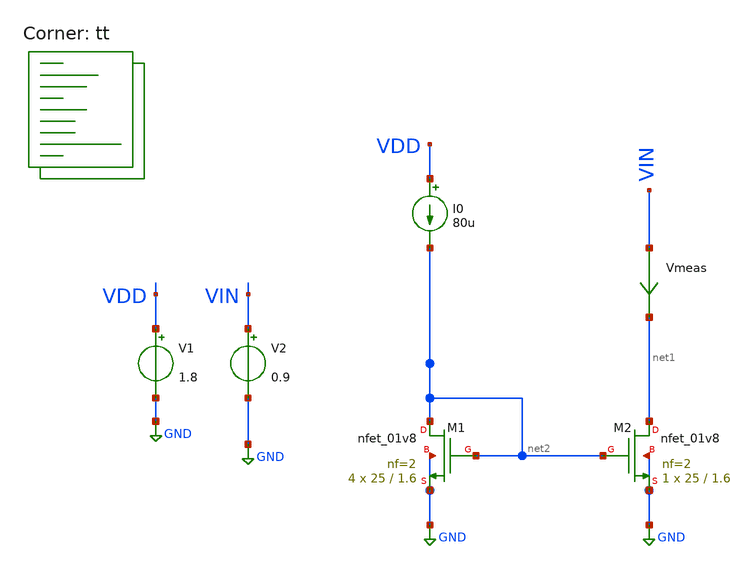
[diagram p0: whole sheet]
** sch_path: sky130B/Analog_integrated_circuit_Design/chapter3/1/1.sch
**.subckt 1
V1 VDD GND 1.8
V2 VIN GND 0.9
Vmeas VIN net1 0
.save i(vmeas)
XM2 net1 net2 GND GND sky130_fd_pr__nfet_01v8 L=1.6 W=25 nf=2 ad='int((2 + 1)/2) * 25 / 2 * 0.29' as='int((2 + 2)/2) * 25 / 2 * 0.29'
+ pd='2*int((2 + 1)/2) * (25 / 2 + 0.29)' ps='2*int((2 + 2)/2) * (25 / 2 + 0.29)' nrd='0.29 / 25 ' nrs='0.29 / 25 '
+ sa=0 sb=0 sd=0 mult=1 m=1
XM1 net2 net2 GND GND sky130_fd_pr__nfet_01v8 L=1.6 W=25 nf=2 ad='int((2 + 1)/2) * 25 / 2 * 0.29' as='int((2 + 2)/2) * 25 / 2 * 0.29'
+ pd='2*int((2 + 1)/2) * (25 / 2 + 0.29)' ps='2*int((2 + 2)/2) * (25 / 2 + 0.29)' nrd='0.29 / 25 ' nrs='0.29 / 25 '
+ sa=0 sb=0 sd=0 mult=4 m=4
I0 VDD net2 80u
**** begin user architecture code
.lib $::SKYWATER_MODELS/sky130.lib.spice tt

**************************************************************
**************************************************************
**************************************************************
**************************************************************
**************************************************************
*LIBs*********************************************************
**************************************************************
**************************************************************
**************************************************************
**************************************************************
**************************************************************
*.lib $::SKYWATER_MODELS/sky130.lib.spice tt
* chose the corners in the corner file
* tt_mm for mismatch
* ss ff sf fs standart corners
* ll hh lh hl capacitor and resistors corners
* mc for total process variation including corners
**************************************************************
**************************************************************
**************************************************************
**************************************************************
**************************************************************
*Corners/montecarlo options***********************************
**************************************************************
**************************************************************
**************************************************************
**************************************************************
**************************************************************
.TEMP 27
**************************************************************
**************************************************************
**************************************************************
**************************************************************
*SIMULATION and Plots*****************************************
**************************************************************
**************************************************************
**************************************************************
**************************************************************
.control
save all
dc V2 0 1.8 0.001
*dc simulation
plot i(Vmeas)
plot 1/deriv(i(Vmeas))
.endc

**** end user architecture code
**.ends
.GLOBAL GND
.end
